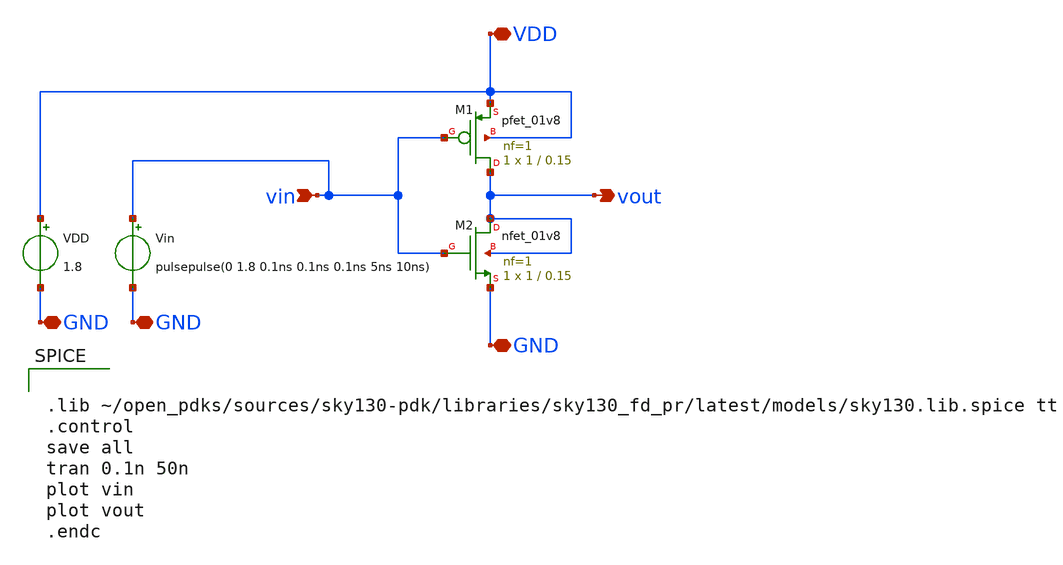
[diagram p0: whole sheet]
** sch_path: Week 0/Spice_Netlist/xschem/inverter.sch
**.subckt inverter vin vout VDD GND GND GND
*.ipin vin
*.opin vout
*.iopin VDD
*.iopin GND
*.iopin GND
*.iopin GND
XM1 vout vin VDD VDD sky130_fd_pr__pfet_01v8 L=0.15 W=1 nf=1 ad='int((nf+1)/2) * W/nf * 0.29' as='int((nf+2)/2) * W/nf * 0.29'
+ pd='2*int((nf+1)/2) * (W/nf + 0.29)' ps='2*int((nf+2)/2) * (W/nf + 0.29)' nrd='0.29 / W' nrs='0.29 / W'
+ sa=0 sb=0 sd=0 mult=1 m=1
XM2 vout vin GND vout sky130_fd_pr__nfet_01v8 L=0.15 W=1 nf=1 ad='int((nf+1)/2) * W/nf * 0.29' as='int((nf+2)/2) * W/nf * 0.29'
+ pd='2*int((nf+1)/2) * (W/nf + 0.29)' ps='2*int((nf+2)/2) * (W/nf + 0.29)' nrd='0.29 / W' nrs='0.29 / W'
+ sa=0 sb=0 sd=0 mult=1 m=1
Vin vin GND pulsepulse(0 1.8 0.1ns 0.1ns 0.1ns 5ns 10ns)
VDD VDD GND 1.8
**** begin user architecture code


.lib ~/open_pdks/sources/sky130-pdk/libraries/sky130_fd_pr/latest/models/sky130.lib.spice tt
.control
save all
tran 0.1n 50n
plot vin
plot vout
.endc

**** end user architecture code
**.ends
.end
